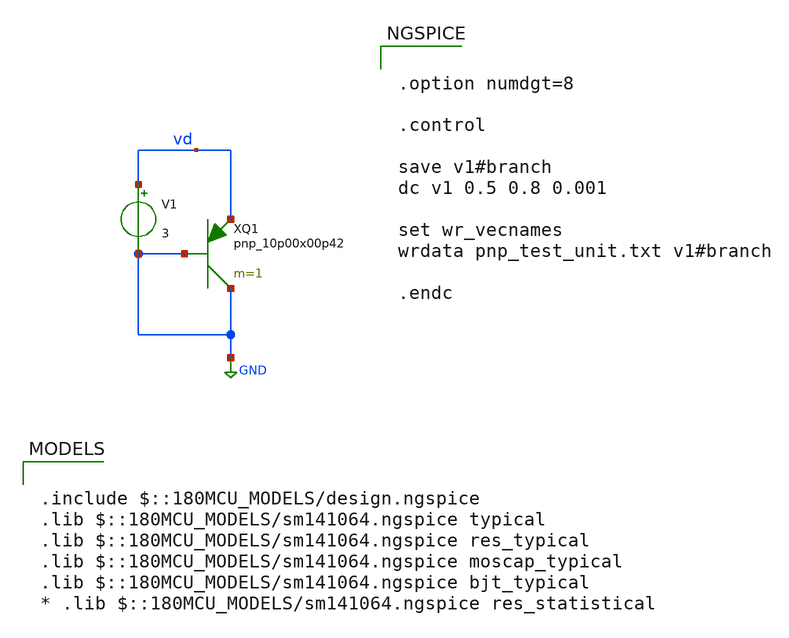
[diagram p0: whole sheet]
** sch_path: designs/switch_matrix_gf180mcu_9t5v0-main/designs/libs/core_analog/vref/pnp_test_unit.sch
**.subckt pnp_test_unit
XQ1 GND GND vd pnp_10p00x00p42 m=1 par=1
V1 vd GND 3
**** begin user architecture code

.include $::180MCU_MODELS/design.ngspice
.lib $::180MCU_MODELS/sm141064.ngspice typical
.lib $::180MCU_MODELS/sm141064.ngspice res_typical
.lib $::180MCU_MODELS/sm141064.ngspice moscap_typical
.lib $::180MCU_MODELS/sm141064.ngspice bjt_typical
* .lib $::180MCU_MODELS/sm141064.ngspice res_statistical



.option numdgt=8

.control

save v1#branch
dc v1 0.5 0.8 0.001

set wr_vecnames
wrdata pnp_test_unit.txt v1#branch

.endc


**** end user architecture code
**.ends
.GLOBAL GND
.end
